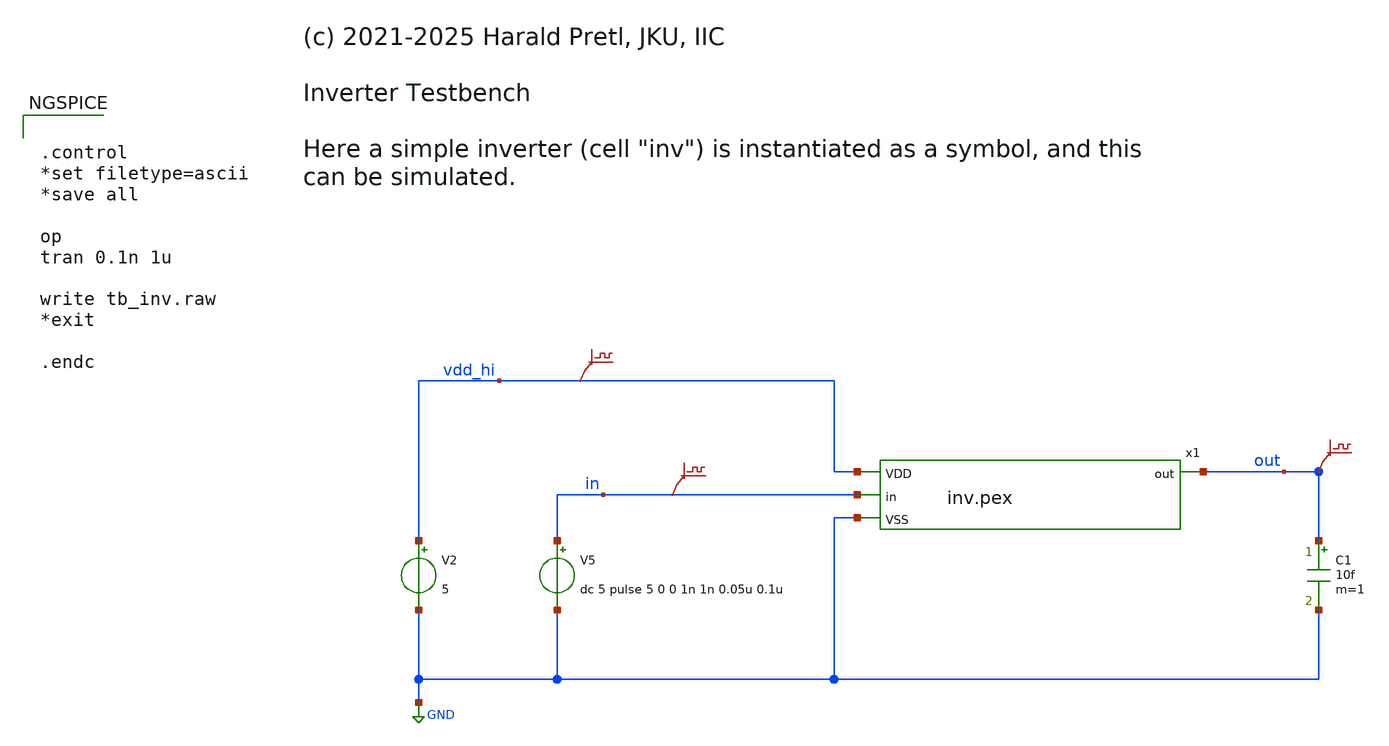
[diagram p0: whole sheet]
** sch_path: _build/images/iic-osic-tools/skel/foss/examples/demo_sky130A/ana/tb_inv_pex.sch
* (c) 2021-2025 Harald Pretl, JKU, IIC
* (c) 2024 Harald Pretl, IIC@JKU
**.subckt tb_inv_pex
V2 vdd_hi GND 5
V5 in GND dc 5 pulse 5 0 0 1n 1n 0.05u 0.1u
x1 vdd_hi in out GND inv.pex
C1 out GND 10f m=1
.save v(vdd_hi)
.save v(in)
.save v(out)
**** begin user architecture code
 ** manual skywater pdks install (with patches applied)
* .lib $::SKYWATER_MODELS/models/sky130.lib.spice tt

** opencircuitdesign pdks install
.lib $::SKYWATER_MODELS/sky130.lib.spice.tt.red tt

.param mc_mm_switch=0
.param mc_pr_switch=0



.control
*set filetype=ascii
*save all

op
tran 0.1n 1u

write tb_inv.raw
*exit

.endc


**** end user architecture code
**.ends

* expanding   symbol:  inv.pex.sym # of pins=4
** sym_path: _build/images/iic-osic-tools/skel_eda/foss/examples/demo_sky130A/ana/inv.pex.sym
.include inv.pex.spice
.GLOBAL GND
.end
